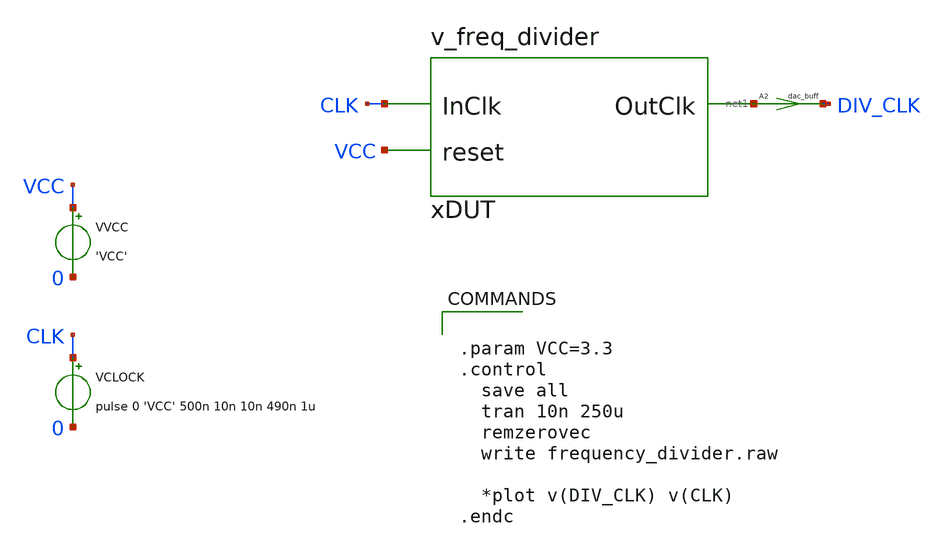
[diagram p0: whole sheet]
** sch_path: sch/design/frequency_divider.sch
**.subckt frequency_divider
xDUT [ CLK VCC ] [ net1 ] dut
VVCC VCC 0 'VCC'
VCLOCK CLK 0 pulse 0 'VCC' 500n 10n 10n 490n 1u
A2 [ net1 ] [ DIV_CLK ] dac_buff
**** begin user architecture code


.param VCC=3.3
.control
  save all
  tran 10n 250u
  remzerovec
  write frequency_divider.raw

  *plot v(DIV_CLK) v(CLK)
.endc


**** end user architecture code
**.ends
**** begin user architecture code
.model dut d_cosim simulation="ivlng" sim_args=["freq_divider"]   vlow=0.8 vhigh=2.0   v0=0 v1=3.3
+   rise=1n fall=1n
.model dac_buff dac_bridge input_load=1e-15 t_rise=10n t_fall=10n  out_low=0 out_high=3.3
**** end user architecture code
.end
